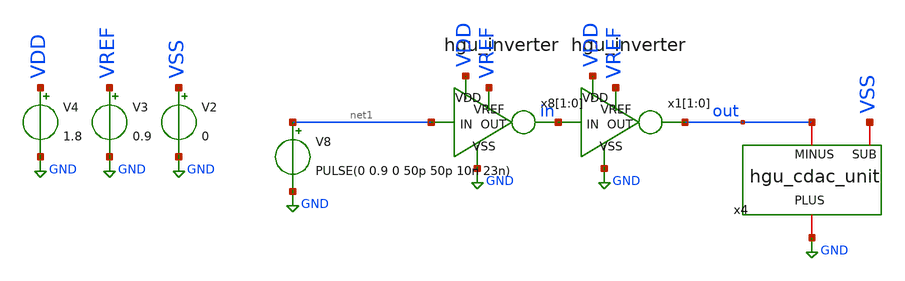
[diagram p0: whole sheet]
** sch_path: hgu/tb/untitled-2.sch
**.subckt untitled-2
x8[1] VDD net1 in GND VREF hgu_inverter
x8[0] VDD net1 in GND VREF hgu_inverter
x4 GND out VSS hgu_cdac_unit
V8 net1 GND PULSE(0 0.9 0 50p 50p 10n 23n)
V2 VSS GND 0
V3 VREF GND 0.9
V4 VDD GND 1.8
x1[1] VDD in out GND VREF hgu_inverter
x1[0] VDD in out GND VREF hgu_inverter
**** begin user architecture code



.OPTIONS savecurrents
.tran 10ps 20ns
.include /foss/designs/hgu_goss/hgu/mag/hgu_cdac_unit.spice
.lib /foss/pdks/sky130A/libs.tech/ngspice/sky130.lib.spice tt
.include /foss/pdks/sky130A/libs.ref/sky130_fd_sc_hd/spice/sky130_fd_sc_hd.spice

.control
	run
	let svdd = 0.9
	let max = svdd*0.8
	let min = svdd*0.2
	let mid = svdd*0.5
	meas tran rising_s1 find time when V(out)=min RISE=1 TD=0.1p
        meas tran rising_e1 find time when V(out)=max RISE=1 TD=0.1p
        let rising_time1 = rising_e1-rising_s1
        meas tran falling_s1 find time when V(out)=max FALL=1 TD=0.1p
        meas tran falling_e1 find time when V(out)=min FALL=1 TD=0.1p
        let falling_time1 = falling_e1-falling_s1

        print rising_time1 falling_time1
	plot v(in) v(out)
.endc
.save all



**** end user architecture code
**.ends
.GLOBAL GND
.end
